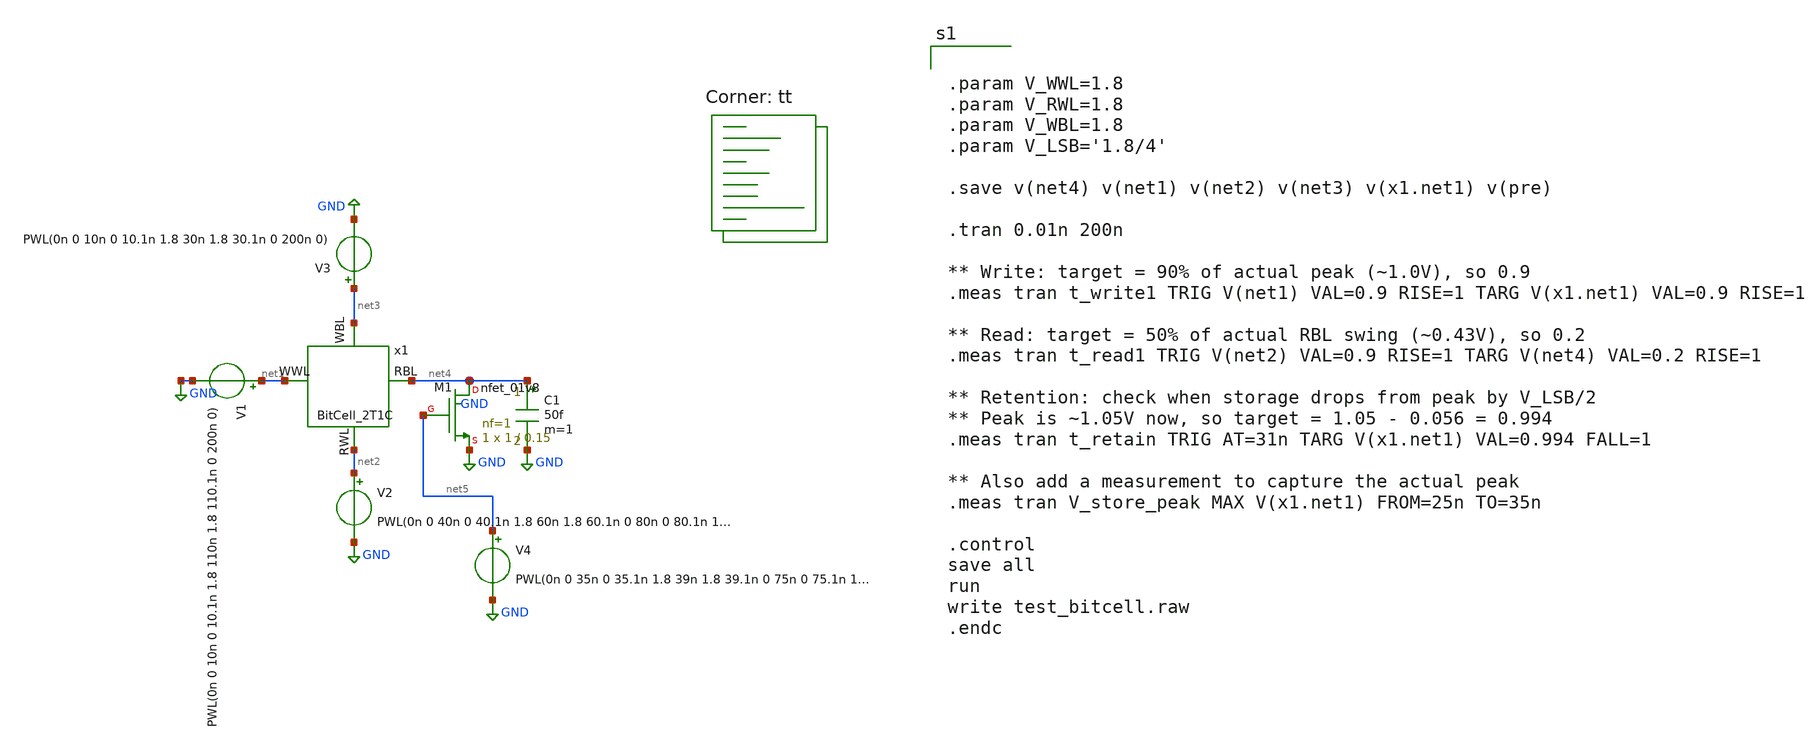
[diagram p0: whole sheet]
** sch_path: analog/schematics/test_bitcell.sch
**.subckt test_bitcell
x1 net4 net1 net3 net2 BitCell_2T1C
V1 net1 GND PWL(0n 0 10n 0 10.1n 1.8 110n 1.8 110.1n 0 200n 0)
V3 net3 GND PWL(0n 0 10n 0 10.1n 1.8 30n 1.8 30.1n 0 200n 0)
C1 net4 GND 50f m=1
V2 net2 GND PWL(0n 0 40n 0 40.1n 1.8 60n 1.8 60.1n 0 80n 0 80.1n 1.8 100n 1.8 100.1n 0 200n 0)
V4 net5 GND PWL(0n 0 35n 0 35.1n 1.8 39n 1.8 39.1n 0 75n 0 75.1n 1.8 79n 1.8 79.1n 0 200n 0)
XM1 net4 net5 GND GND sky130_fd_pr__nfet_01v8 L=0.15 W=1 nf=1 ad='int((nf+1)/2) * W/nf * 0.29' as='int((nf+2)/2) * W/nf * 0.29'
+ pd='2*int((nf+1)/2) * (W/nf + 0.29)' ps='2*int((nf+2)/2) * (W/nf + 0.29)' nrd='0.29 / W' nrs='0.29 / W'
+ sa=0 sb=0 sd=0 mult=1 m=1
**** begin user architecture code


.param V_WWL=1.8
.param V_RWL=1.8
.param V_WBL=1.8
.param V_LSB='1.8/4'

.save v(net4) v(net1) v(net2) v(net3) v(x1.net1) v(pre)

.tran 0.01n 200n

** Write: target = 90% of actual peak (~1.0V), so 0.9
.meas tran t_write1 TRIG V(net1) VAL=0.9 RISE=1 TARG V(x1.net1) VAL=0.9 RISE=1

** Read: target = 50% of actual RBL swing (~0.43V), so 0.2
.meas tran t_read1 TRIG V(net2) VAL=0.9 RISE=1 TARG V(net4) VAL=0.2 RISE=1

** Retention: check when storage drops from peak by V_LSB/2
** Peak is ~1.05V now, so target = 1.05 - 0.056 = 0.994
.meas tran t_retain TRIG AT=31n TARG V(x1.net1) VAL=0.994 FALL=1

** Also add a measurement to capture the actual peak
.meas tran V_store_peak MAX V(x1.net1) FROM=25n TO=35n

.control
save all
run
write test_bitcell.raw
.endc


.lib $::SKYWATER_MODELS/sky130.lib.spice tt
**** end user architecture code
**.ends

* expanding   symbol:  Core/BitCell_2T1C.sym # of pins=4
** sym_path: analog/schematics/Core/BitCell_2T1C.sym
** sch_path: analog/schematics/Core/BitCell_2T1C.sch
.subckt BitCell_2T1C RBL WWL WBL RWL
*.ipin WBL
*.ipin RWL
*.ipin WWL
*.opin RBL
XM1 net1 WWL WBL GND sky130_fd_pr__nfet_01v8 L=0.5 W=0.36 nf=1 ad='int((nf+1)/2) * W/nf * 0.29' as='int((nf+2)/2) * W/nf * 0.29'
+ pd='2*int((nf+1)/2) * (W/nf + 0.29)' ps='2*int((nf+2)/2) * (W/nf + 0.29)' nrd='0.29 / W' nrs='0.29 / W'
+ sa=0 sb=0 sd=0 mult=1 m=1
XM2 RBL net1 RWL GND sky130_fd_pr__nfet_01v8 L=0.15 W=1 nf=1 ad='int((nf+1)/2) * W/nf * 0.29' as='int((nf+2)/2) * W/nf * 0.29'
+ pd='2*int((nf+1)/2) * (W/nf + 0.29)' ps='2*int((nf+2)/2) * (W/nf + 0.29)' nrd='0.29 / W' nrs='0.29 / W'
+ sa=0 sb=0 sd=0 mult=1 m=1
XC1 net1 GND sky130_fd_pr__cap_mim_m3_1 W=10 L=10 MF=1 m=1
.ends

.GLOBAL GND
.end
